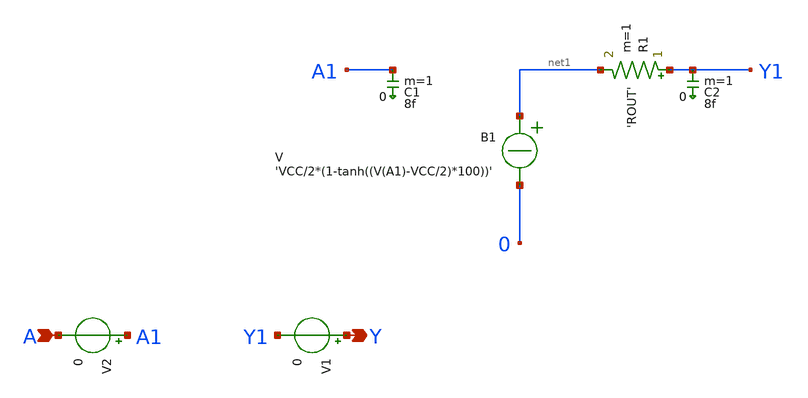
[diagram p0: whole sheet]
** sch_path: xschem_library/ngspice/inv_ngspice.sch
* Copyright (C) 1998-2023 Stefan Frederik Schippers
* This program is free software; you can redistribute it and/or modify
* it under the terms of the GNU General Public License as published by
* the Free Software Foundation; either version 2 of the License, or
* (at your option) any later version.
* This program is distributed in the hope that it will be useful,
* but WITHOUT ANY WARRANTY; without even the implied warranty of
* MERCHANTABILITY or FITNESS FOR A PARTICULAR PURPOSE.  See the
* GNU General Public License for more details.
* You should have received a copy of the GNU General Public License
* along with this program; if not, write to the Free Software
**.subckt inv_ngspice A Y
*.ipin A
*.opin Y
B1 net1 0 V = 'VCC/2*(1-tanh((V(A1)-VCC/2)*100))'
R1 Y1 net1 'ROUT' m=1
C1 A1 0 8f m=1
C2 Y1 0 8f m=1
V1 Y Y1 0
.save i(v1)
V2 A1 A 0
.save i(v2)
**.ends
.end
